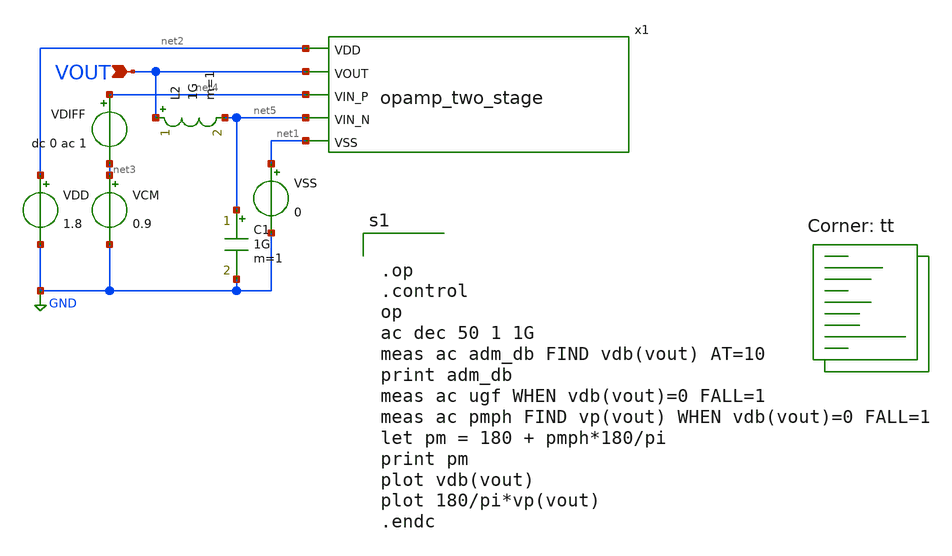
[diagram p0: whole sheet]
** sch_path: analog/bootcamp_opamp/schematics/tb_ac_analysis.sch
**.subckt tb_ac_analysis VOUT
*.ipin VOUT
VDD net2 GND 1.8
VSS net1 GND 0
VCM net3 GND 0.9
VDIFF net4 net3 dc 0 ac 1
x1 net2 VOUT net4 net5 net1 opamp_two_stage
L2 VOUT net5 1G m=1
C1 net5 GND 1G m=1
**** begin user architecture code


.op
.control
op
ac dec 50 1 1G
meas ac adm_db FIND vdb(vout) AT=10
print adm_db
meas ac ugf WHEN vdb(vout)=0 FALL=1
meas ac pmph FIND vp(vout) WHEN vdb(vout)=0 FALL=1
let pm = 180 + pmph*180/pi
print pm
plot vdb(vout)
plot 180/pi*vp(vout)
.endc

.lib $::SKYWATER_MODELS/sky130.lib.spice tt
**** end user architecture code
**.ends

* expanding   symbol:  opamp_two_stage.sym # of pins=5
** sym_path: analog/bootcamp_opamp/schematics/opamp_two_stage.sym
** sch_path: analog/bootcamp_opamp/schematics/opamp_two_stage.sch
.subckt opamp_two_stage VDD VOUT VIN_P VIN_N VSS
*.ipin VIN_N
*.ipin VIN_P
*.ipin VDD
*.ipin VSS
*.ipin VOUT
XMN1 net2 VIN_N net1 VSS sky130_fd_pr__nfet_01v8 L=1 W=20 nf=1 ad='int((nf+1)/2) * W/nf * 0.29' as='int((nf+2)/2) * W/nf * 0.29'
+ pd='2*int((nf+1)/2) * (W/nf + 0.29)' ps='2*int((nf+2)/2) * (W/nf + 0.29)' nrd='0.29 / W' nrs='0.29 / W'
+ sa=0 sb=0 sd=0 mult=1 m=1
XMP1 net2 net2 VDD VDD sky130_fd_pr__pfet_01v8 L=1 W=10 nf=1 ad='int((nf+1)/2) * W/nf * 0.29' as='int((nf+2)/2) * W/nf * 0.29'
+ pd='2*int((nf+1)/2) * (W/nf + 0.29)' ps='2*int((nf+2)/2) * (W/nf + 0.29)' nrd='0.29 / W' nrs='0.29 / W'
+ sa=0 sb=0 sd=0 mult=1 m=1
XMP2 net3 net2 VDD VDD sky130_fd_pr__pfet_01v8 L=1 W=10 nf=1 ad='int((nf+1)/2) * W/nf * 0.29' as='int((nf+2)/2) * W/nf * 0.29'
+ pd='2*int((nf+1)/2) * (W/nf + 0.29)' ps='2*int((nf+2)/2) * (W/nf + 0.29)' nrd='0.29 / W' nrs='0.29 / W'
+ sa=0 sb=0 sd=0 mult=1 m=1
XMN2 net3 VIN_P net1 VSS sky130_fd_pr__nfet_01v8 L=1 W=20 nf=1 ad='int((nf+1)/2) * W/nf * 0.29' as='int((nf+2)/2) * W/nf * 0.29'
+ pd='2*int((nf+1)/2) * (W/nf + 0.29)' ps='2*int((nf+2)/2) * (W/nf + 0.29)' nrd='0.29 / W' nrs='0.29 / W'
+ sa=0 sb=0 sd=0 mult=1 m=1
XMNB net1 net5 VSS VSS sky130_fd_pr__nfet_01v8 L=1 W=4 nf=1 ad='int((nf+1)/2) * W/nf * 0.29' as='int((nf+2)/2) * W/nf * 0.29'
+ pd='2*int((nf+1)/2) * (W/nf + 0.29)' ps='2*int((nf+2)/2) * (W/nf + 0.29)' nrd='0.29 / W' nrs='0.29 / W'
+ sa=0 sb=0 sd=0 mult=2 m=2
XMPO VOUT net3 VDD VDD sky130_fd_pr__pfet_01v8 L=0.15 W=15 nf=1 ad='int((nf+1)/2) * W/nf * 0.29' as='int((nf+2)/2) * W/nf * 0.29'
+ pd='2*int((nf+1)/2) * (W/nf + 0.29)' ps='2*int((nf+2)/2) * (W/nf + 0.29)' nrd='0.29 / W' nrs='0.29 / W'
+ sa=0 sb=0 sd=0 mult=8 m=8
XR1 net4 net3 sky130_fd_pr__res_generic_po W=1 L=2.5 m=1
XC1 net4 VOUT sky130_fd_pr__cap_mim_m3_1 W=22 L=22 MF=1 m=1
XMB VOUT net5 VSS VSS sky130_fd_pr__nfet_01v8 L=0.15 W=6 nf=1 ad='int((nf+1)/2) * W/nf * 0.29' as='int((nf+2)/2) * W/nf * 0.29'
+ pd='2*int((nf+1)/2) * (W/nf + 0.29)' ps='2*int((nf+2)/2) * (W/nf + 0.29)' nrd='0.29 / W' nrs='0.29 / W'
+ sa=0 sb=0 sd=0 mult=8 m=8
XR2 net5 VDD VSS sky130_fd_pr__res_xhigh_po_0p69 L=16 mult=1 m=1
XMB1 net5 net5 VSS VSS sky130_fd_pr__nfet_01v8 L=1 W=4 nf=1 ad='int((nf+1)/2) * W/nf * 0.29' as='int((nf+2)/2) * W/nf * 0.29'
+ pd='2*int((nf+1)/2) * (W/nf + 0.29)' ps='2*int((nf+2)/2) * (W/nf + 0.29)' nrd='0.29 / W' nrs='0.29 / W'
+ sa=0 sb=0 sd=0 mult=1 m=1
.ends

.GLOBAL GND
.end
